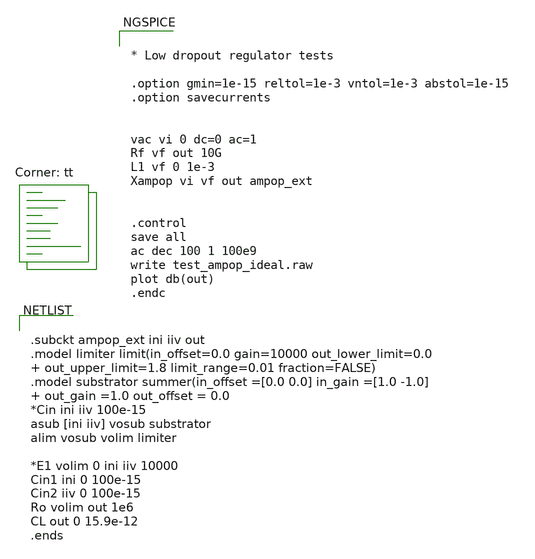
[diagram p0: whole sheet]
** sch_path: xschem/test_ampop_ideal.sch
**.subckt test_ampop_ideal
**** begin user architecture code


.subckt ampop_ext ini iiv out
.model limiter limit(in_offset=0.0 gain=10000 out_lower_limit=0.0  out_upper_limit=1.8
+ limit_range=0.01 fraction=FALSE)
.model substrator summer(in_offset =[0.0 0.0] in_gain =[1.0 -1.0]  out_gain =1.0 out_offset = 0.0
*Cin ini iiv 100e-15
asub [ini iiv] vosub substrator
alim vosub volim limiter

*E1 volim 0 ini iiv 10000
Cin1 ini 0 100e-15
Cin2 iiv 0 100e-15
Ro volim out 1e6
CL out 0 15.9e-12
.ends




* Low dropout regulator tests

.option gmin=1e-15 reltol=1e-3 vntol=1e-3 abstol=1e-15
.option savecurrents


vac vi 0 dc=0 ac=1
Rf vf out 10G
L1 vf 0 1e-3
Xampop vi vf out ampop_ext


.control
save all
ac dec 100 1 100e9
write test_ampop_ideal.raw
plot db(out)
.endc


.lib $::SKYWATER_MODELS/sky130.lib.spice tt
**** end user architecture code
**.ends
.end
